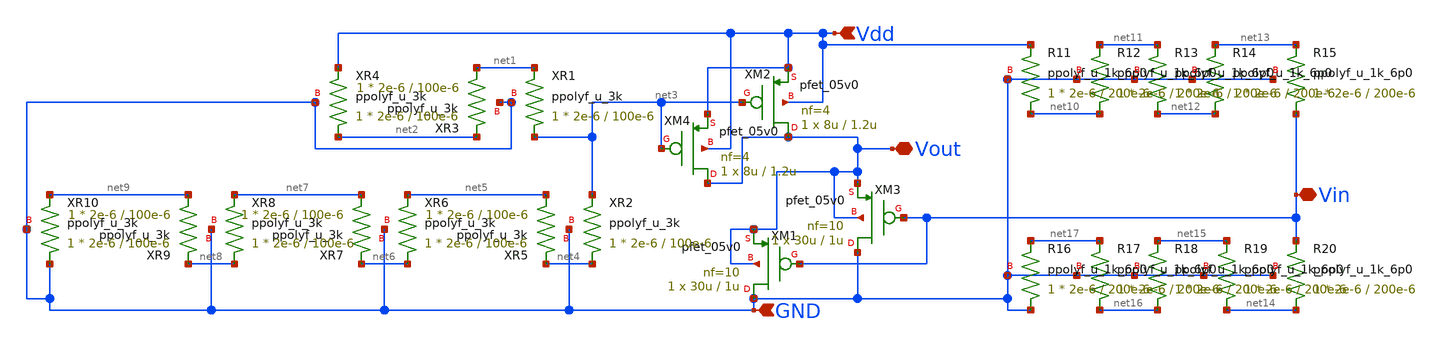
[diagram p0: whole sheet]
** sch_path: RN_buffer/buffer.sch
**.subckt buffer Vdd GND Vin Vout
*.ipin Vdd
*.ipin GND
*.iopin Vin
*.iopin Vout
XM1 GND Vin Vout Vout pfet_05v0 L=1u W=30u nf=10 ad='int((nf+1)/2) * W/nf * 0.18u' as='int((nf+2)/2) * W/nf * 0.18u'
+ pd='2*int((nf+1)/2) * (W/nf + 0.18u)' ps='2*int((nf+2)/2) * (W/nf + 0.18u)' nrd='0.18u / W' nrs='0.18u / W'
+ sa=0 sb=0 sd=0 m=1
XR1 net3 net1 GND ppolyf_u_3k r_width=2e-6 r_length=100e-6 m=1
XR2 net4 net3 GND ppolyf_u_3k r_width=2e-6 r_length=100e-6 m=1
XM2 Vout net3 Vdd Vdd pfet_05v0 L=1.2u W=8u nf=4 ad='int((nf+1)/2) * W/nf * 0.18u' as='int((nf+2)/2) * W/nf * 0.18u'
+ pd='2*int((nf+1)/2) * (W/nf + 0.18u)' ps='2*int((nf+2)/2) * (W/nf + 0.18u)' nrd='0.18u / W' nrs='0.18u / W'
+ sa=0 sb=0 sd=0 m=1
XR3 net1 net2 GND ppolyf_u_3k r_width=2e-6 r_length=100e-6 m=1
XR4 net2 Vdd GND ppolyf_u_3k r_width=2e-6 r_length=100e-6 m=1
XR5 net5 net4 GND ppolyf_u_3k r_width=2e-6 r_length=100e-6 m=1
XR6 net6 net5 GND ppolyf_u_3k r_width=2e-6 r_length=100e-6 m=1
XR7 net7 net6 GND ppolyf_u_3k r_width=2e-6 r_length=100e-6 m=1
XR8 net8 net7 GND ppolyf_u_3k r_width=2e-6 r_length=100e-6 m=1
XR9 net9 net8 GND ppolyf_u_3k r_width=2e-6 r_length=100e-6 m=1
XR10 GND net9 GND ppolyf_u_3k r_width=2e-6 r_length=100e-6 m=1
XM3 GND Vin Vout Vout pfet_05v0 L=1u W=30u nf=10 ad='int((nf+1)/2) * W/nf * 0.18u' as='int((nf+2)/2) * W/nf * 0.18u'
+ pd='2*int((nf+1)/2) * (W/nf + 0.18u)' ps='2*int((nf+2)/2) * (W/nf + 0.18u)' nrd='0.18u / W' nrs='0.18u / W'
+ sa=0 sb=0 sd=0 m=1
XM4 Vout net3 Vdd Vdd pfet_05v0 L=1.2u W=8u nf=4 ad='int((nf+1)/2) * W/nf * 0.18u' as='int((nf+2)/2) * W/nf * 0.18u'
+ pd='2*int((nf+1)/2) * (W/nf + 0.18u)' ps='2*int((nf+2)/2) * (W/nf + 0.18u)' nrd='0.18u / W' nrs='0.18u / W'
+ sa=0 sb=0 sd=0 m=1
XR11 net10 Vdd GND ppolyf_u_1k_6p0 r_width=2e-6 r_length=200e-6 m=1
XR12 net10 net11 GND ppolyf_u_1k_6p0 r_width=2e-6 r_length=200e-6 m=1
XR13 net12 net11 GND ppolyf_u_1k_6p0 r_width=2e-6 r_length=200e-6 m=1
XR14 net12 net13 GND ppolyf_u_1k_6p0 r_width=2e-6 r_length=200e-6 m=1
XR15 Vin net13 GND ppolyf_u_1k_6p0 r_width=2e-6 r_length=200e-6 m=1
XR16 GND net17 GND ppolyf_u_1k_6p0 r_width=2e-6 r_length=200e-6 m=1
XR17 net16 net17 GND ppolyf_u_1k_6p0 r_width=2e-6 r_length=200e-6 m=1
XR18 net16 net15 GND ppolyf_u_1k_6p0 r_width=2e-6 r_length=200e-6 m=1
XR19 net14 net15 GND ppolyf_u_1k_6p0 r_width=2e-6 r_length=200e-6 m=1
XR20 net14 Vin GND ppolyf_u_1k_6p0 r_width=2e-6 r_length=200e-6 m=1
**.ends
.end
